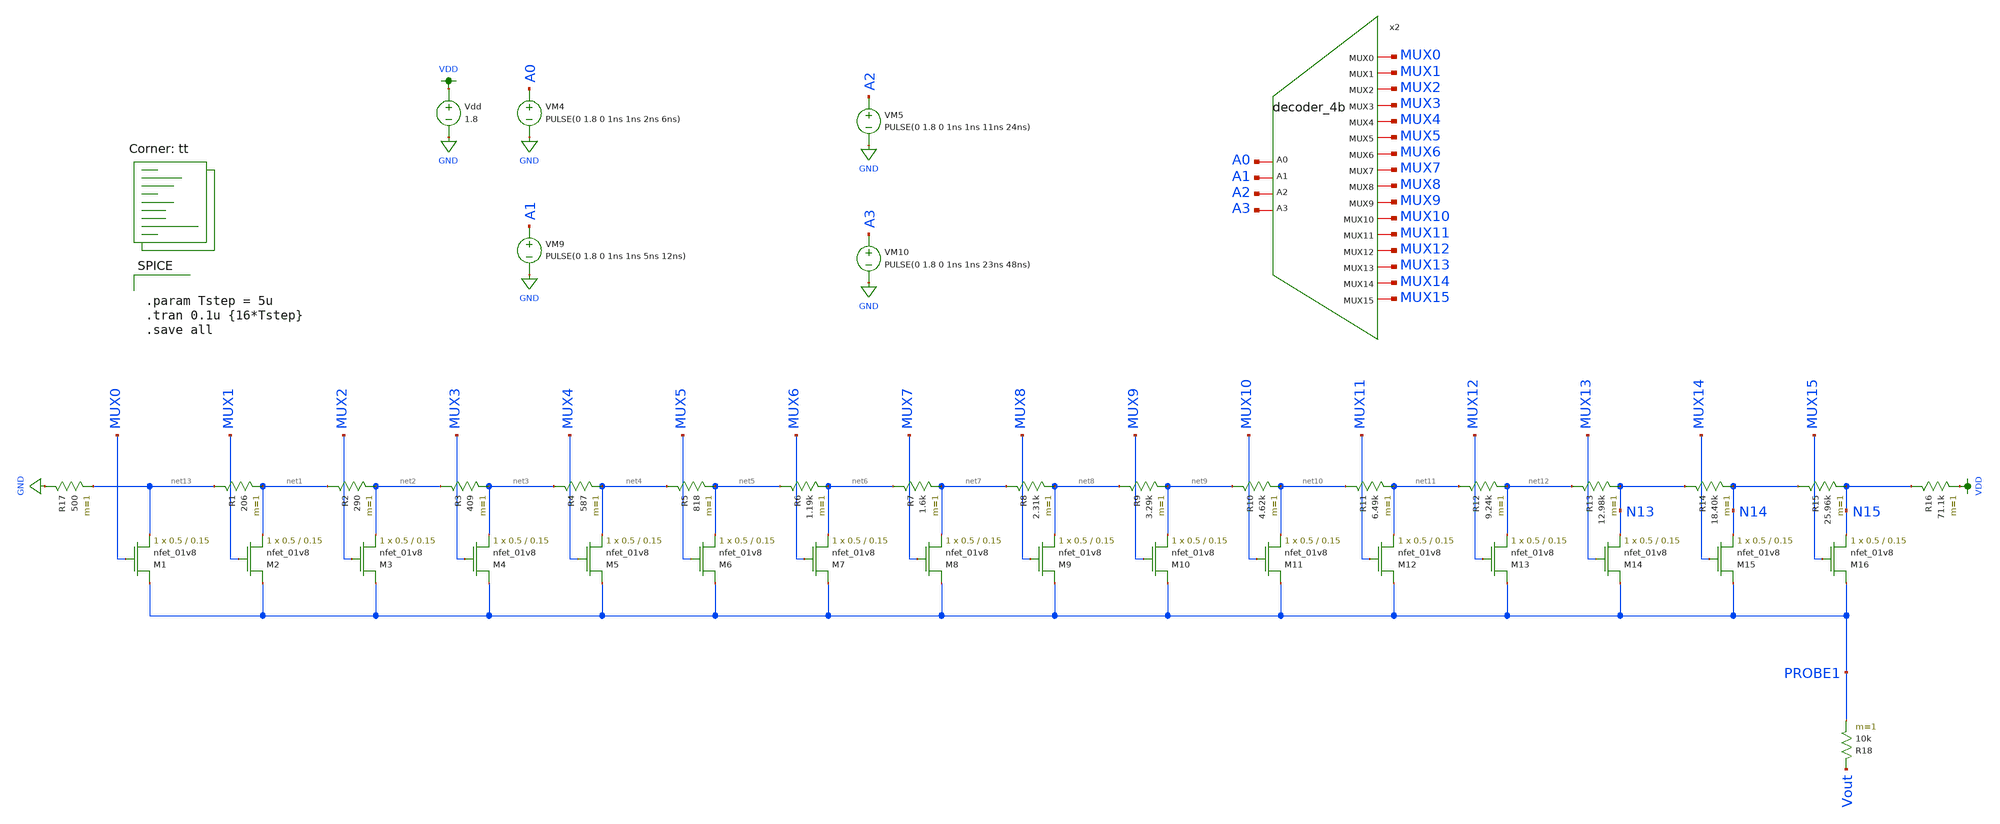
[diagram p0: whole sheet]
** sch_path: DAC/DAC2TB.sch
**.subckt DAC2TB
Vdd VDD GND 1.8
R1 net13 net1 206 m=1
R2 net1 net2 290 m=1
R3 net2 net3 409 m=1
R4 net3 net4 587 m=1
R5 net4 net5 818 m=1
R6 net5 net6 1.19k m=1
R7 net6 net7 1.6k m=1
R8 net7 net8 2.31k m=1
R9 net8 net9 3.29k m=1
R10 net9 net10 4.62k m=1
R11 net10 net11 6.49k m=1
R12 net11 net12 9.24k m=1
R13 net12 N13 12.98k m=1
R14 N13 N14 18.40k m=1
R15 N14 N15 25.96k m=1
R16 N15 VDD 71.1k m=1
XM1 PROBE1 MUX0 net13 GND sky130_fd_pr__nfet_01v8 L=0.15 W=0.5 nf=1 ad='int((nf+1)/2) * W/nf * 0.29'
+ as='int((nf+2)/2) * W/nf * 0.29' pd='2*int((nf+1)/2) * (W/nf + 0.29)' ps='2*int((nf+2)/2) * (W/nf + 0.29)'
+ nrd='0.29 / W' nrs='0.29 / W' sa=0 sb=0 sd=0 mult=1 m=1
VM4 A0 GND PULSE(0 1.8 0 1ns 1ns 2ns 6ns)
VM5 A2 GND PULSE(0 1.8 0 1ns 1ns 11ns 24ns)
VM9 A1 GND PULSE(0 1.8 0 1ns 1ns 5ns 12ns)
VM10 A3 GND PULSE(0 1.8 0 1ns 1ns 23ns 48ns)
R17 GND net13 500 m=1
R18 Vout PROBE1 10k m=1
XM2 PROBE1 MUX1 net1 GND sky130_fd_pr__nfet_01v8 L=0.15 W=0.5 nf=1 ad='int((nf+1)/2) * W/nf * 0.29' as='int((nf+2)/2) * W/nf * 0.29'
+ pd='2*int((nf+1)/2) * (W/nf + 0.29)' ps='2*int((nf+2)/2) * (W/nf + 0.29)' nrd='0.29 / W' nrs='0.29 / W'
+ sa=0 sb=0 sd=0 mult=1 m=1
XM3 PROBE1 MUX2 net2 GND sky130_fd_pr__nfet_01v8 L=0.15 W=0.5 nf=1 ad='int((nf+1)/2) * W/nf * 0.29' as='int((nf+2)/2) * W/nf * 0.29'
+ pd='2*int((nf+1)/2) * (W/nf + 0.29)' ps='2*int((nf+2)/2) * (W/nf + 0.29)' nrd='0.29 / W' nrs='0.29 / W'
+ sa=0 sb=0 sd=0 mult=1 m=1
XM4 PROBE1 MUX3 net3 GND sky130_fd_pr__nfet_01v8 L=0.15 W=0.5 nf=1 ad='int((nf+1)/2) * W/nf * 0.29' as='int((nf+2)/2) * W/nf * 0.29'
+ pd='2*int((nf+1)/2) * (W/nf + 0.29)' ps='2*int((nf+2)/2) * (W/nf + 0.29)' nrd='0.29 / W' nrs='0.29 / W'
+ sa=0 sb=0 sd=0 mult=1 m=1
XM5 PROBE1 MUX4 net4 GND sky130_fd_pr__nfet_01v8 L=0.15 W=0.5 nf=1 ad='int((nf+1)/2) * W/nf * 0.29' as='int((nf+2)/2) * W/nf * 0.29'
+ pd='2*int((nf+1)/2) * (W/nf + 0.29)' ps='2*int((nf+2)/2) * (W/nf + 0.29)' nrd='0.29 / W' nrs='0.29 / W'
+ sa=0 sb=0 sd=0 mult=1 m=1
XM6 PROBE1 MUX5 net5 GND sky130_fd_pr__nfet_01v8 L=0.15 W=0.5 nf=1 ad='int((nf+1)/2) * W/nf * 0.29' as='int((nf+2)/2) * W/nf * 0.29'
+ pd='2*int((nf+1)/2) * (W/nf + 0.29)' ps='2*int((nf+2)/2) * (W/nf + 0.29)' nrd='0.29 / W' nrs='0.29 / W'
+ sa=0 sb=0 sd=0 mult=1 m=1
XM7 PROBE1 MUX6 net6 GND sky130_fd_pr__nfet_01v8 L=0.15 W=0.5 nf=1 ad='int((nf+1)/2) * W/nf * 0.29' as='int((nf+2)/2) * W/nf * 0.29'
+ pd='2*int((nf+1)/2) * (W/nf + 0.29)' ps='2*int((nf+2)/2) * (W/nf + 0.29)' nrd='0.29 / W' nrs='0.29 / W'
+ sa=0 sb=0 sd=0 mult=1 m=1
XM8 PROBE1 MUX7 net7 GND sky130_fd_pr__nfet_01v8 L=0.15 W=0.5 nf=1 ad='int((nf+1)/2) * W/nf * 0.29' as='int((nf+2)/2) * W/nf * 0.29'
+ pd='2*int((nf+1)/2) * (W/nf + 0.29)' ps='2*int((nf+2)/2) * (W/nf + 0.29)' nrd='0.29 / W' nrs='0.29 / W'
+ sa=0 sb=0 sd=0 mult=1 m=1
XM9 PROBE1 MUX8 net8 GND sky130_fd_pr__nfet_01v8 L=0.15 W=0.5 nf=1 ad='int((nf+1)/2) * W/nf * 0.29' as='int((nf+2)/2) * W/nf * 0.29'
+ pd='2*int((nf+1)/2) * (W/nf + 0.29)' ps='2*int((nf+2)/2) * (W/nf + 0.29)' nrd='0.29 / W' nrs='0.29 / W'
+ sa=0 sb=0 sd=0 mult=1 m=1
XM10 PROBE1 MUX9 net9 GND sky130_fd_pr__nfet_01v8 L=0.15 W=0.5 nf=1 ad='int((nf+1)/2) * W/nf * 0.29'
+ as='int((nf+2)/2) * W/nf * 0.29' pd='2*int((nf+1)/2) * (W/nf + 0.29)' ps='2*int((nf+2)/2) * (W/nf + 0.29)'
+ nrd='0.29 / W' nrs='0.29 / W' sa=0 sb=0 sd=0 mult=1 m=1
XM11 PROBE1 MUX10 net10 GND sky130_fd_pr__nfet_01v8 L=0.15 W=0.5 nf=1 ad='int((nf+1)/2) * W/nf * 0.29'
+ as='int((nf+2)/2) * W/nf * 0.29' pd='2*int((nf+1)/2) * (W/nf + 0.29)' ps='2*int((nf+2)/2) * (W/nf + 0.29)'
+ nrd='0.29 / W' nrs='0.29 / W' sa=0 sb=0 sd=0 mult=1 m=1
XM12 PROBE1 MUX11 net11 GND sky130_fd_pr__nfet_01v8 L=0.15 W=0.5 nf=1 ad='int((nf+1)/2) * W/nf * 0.29'
+ as='int((nf+2)/2) * W/nf * 0.29' pd='2*int((nf+1)/2) * (W/nf + 0.29)' ps='2*int((nf+2)/2) * (W/nf + 0.29)'
+ nrd='0.29 / W' nrs='0.29 / W' sa=0 sb=0 sd=0 mult=1 m=1
XM13 PROBE1 MUX12 net12 GND sky130_fd_pr__nfet_01v8 L=0.15 W=0.5 nf=1 ad='int((nf+1)/2) * W/nf * 0.29'
+ as='int((nf+2)/2) * W/nf * 0.29' pd='2*int((nf+1)/2) * (W/nf + 0.29)' ps='2*int((nf+2)/2) * (W/nf + 0.29)'
+ nrd='0.29 / W' nrs='0.29 / W' sa=0 sb=0 sd=0 mult=1 m=1
XM14 PROBE1 MUX13 N13 GND sky130_fd_pr__nfet_01v8 L=0.15 W=0.5 nf=1 ad='int((nf+1)/2) * W/nf * 0.29'
+ as='int((nf+2)/2) * W/nf * 0.29' pd='2*int((nf+1)/2) * (W/nf + 0.29)' ps='2*int((nf+2)/2) * (W/nf + 0.29)'
+ nrd='0.29 / W' nrs='0.29 / W' sa=0 sb=0 sd=0 mult=1 m=1
XM15 PROBE1 MUX14 N14 GND sky130_fd_pr__nfet_01v8 L=0.15 W=0.5 nf=1 ad='int((nf+1)/2) * W/nf * 0.29'
+ as='int((nf+2)/2) * W/nf * 0.29' pd='2*int((nf+1)/2) * (W/nf + 0.29)' ps='2*int((nf+2)/2) * (W/nf + 0.29)'
+ nrd='0.29 / W' nrs='0.29 / W' sa=0 sb=0 sd=0 mult=1 m=1
XM16 PROBE1 MUX15 N15 GND sky130_fd_pr__nfet_01v8 L=0.15 W=0.5 nf=1 ad='int((nf+1)/2) * W/nf * 0.29'
+ as='int((nf+2)/2) * W/nf * 0.29' pd='2*int((nf+1)/2) * (W/nf + 0.29)' ps='2*int((nf+2)/2) * (W/nf + 0.29)'
+ nrd='0.29 / W' nrs='0.29 / W' sa=0 sb=0 sd=0 mult=1 m=1
x2 A3 A2 A0 A1 MUX0 MUX1 MUX2 MUX3 MUX4 MUX5 MUX6 MUX7 MUX8 MUX9 MUX10 MUX11 MUX12 MUX13 MUX14 MUX15
+ decoder_4b
**** begin user architecture code


.param Tstep = 5u
.tran 0.1u {16*Tstep}
.save all

.lib $::SKYWATER_MODELS/sky130.lib.spice tt
**** end user architecture code
**.ends

* expanding   symbol:  /home/madvlsi/SKY130-AY38910/DAC/decoder_4b.sym # of pins=20
** sym_path: DAC/decoder_4b.sym
** sch_path: DAC/decoder_4b.sch
.subckt decoder_4b A3 A2 A0 A1 MUX0 MUX1 MUX2 MUX3 MUX4 MUX5 MUX6 MUX7 MUX8 MUX9 MUX10 MUX11 MUX12
+ MUX13 MUX14 MUX15
*.iopin MUX0
*.iopin MUX1
*.iopin MUX2
*.iopin MUX3
*.iopin MUX4
*.iopin MUX5
*.iopin MUX6
*.iopin MUX7
*.iopin MUX8
*.iopin MUX9
*.iopin MUX10
*.iopin MUX11
*.iopin MUX12
*.iopin MUX13
*.iopin MUX14
*.iopin MUX15
*.ipin A0
*.ipin A1
*.ipin A2
*.ipin A3
x50 A0 VGND VNB VPB VPWR net1 sky130_fd_sc_hd__inv_1
x1 A1 VGND VNB VPB VPWR net2 sky130_fd_sc_hd__inv_1
x2 A2 VGND VNB VPB VPWR net3 sky130_fd_sc_hd__inv_1
x3 A3 VGND VNB VPB VPWR net4 sky130_fd_sc_hd__inv_1
x4 net1 net2 net3 net4 VGND VNB VPB VPWR MUX0 sky130_fd_sc_hd__and4_1
x5 A0 net2 net3 net4 VGND VNB VPB VPWR MUX1 sky130_fd_sc_hd__and4_1
x6 net1 A1 net3 net4 VGND VNB VPB VPWR MUX2 sky130_fd_sc_hd__and4_1
x7 A0 A1 net3 net4 VGND VNB VPB VPWR MUX3 sky130_fd_sc_hd__and4_1
x9 net1 net2 A2 net4 VGND VNB VPB VPWR MUX4 sky130_fd_sc_hd__and4_1
x10 A0 net2 A2 net4 VGND VNB VPB VPWR MUX5 sky130_fd_sc_hd__and4_1
x11 net1 A1 A2 net4 VGND VNB VPB VPWR MUX6 sky130_fd_sc_hd__and4_1
x12 A0 A1 A2 net4 VGND VNB VPB VPWR MUX7 sky130_fd_sc_hd__and4_1
x14 net1 net2 net3 A3 VGND VNB VPB VPWR MUX8 sky130_fd_sc_hd__and4_1
x15 A0 net2 net3 A3 VGND VNB VPB VPWR MUX9 sky130_fd_sc_hd__and4_1
x16 net1 A1 net3 A3 VGND VNB VPB VPWR MUX10 sky130_fd_sc_hd__and4_1
x17 A0 A1 net3 A3 VGND VNB VPB VPWR MUX11 sky130_fd_sc_hd__and4_1
x19 net1 net2 A2 A3 VGND VNB VPB VPWR MUX12 sky130_fd_sc_hd__and4_1
x20 A0 net2 A2 A3 VGND VNB VPB VPWR MUX13 sky130_fd_sc_hd__and4_1
x21 net1 A1 A2 A3 VGND VNB VPB VPWR MUX14 sky130_fd_sc_hd__and4_1
x22 A0 A1 A2 A3 VGND VNB VPB VPWR MUX15 sky130_fd_sc_hd__and4_1
.ends

.GLOBAL GND
.GLOBAL VDD
.end
